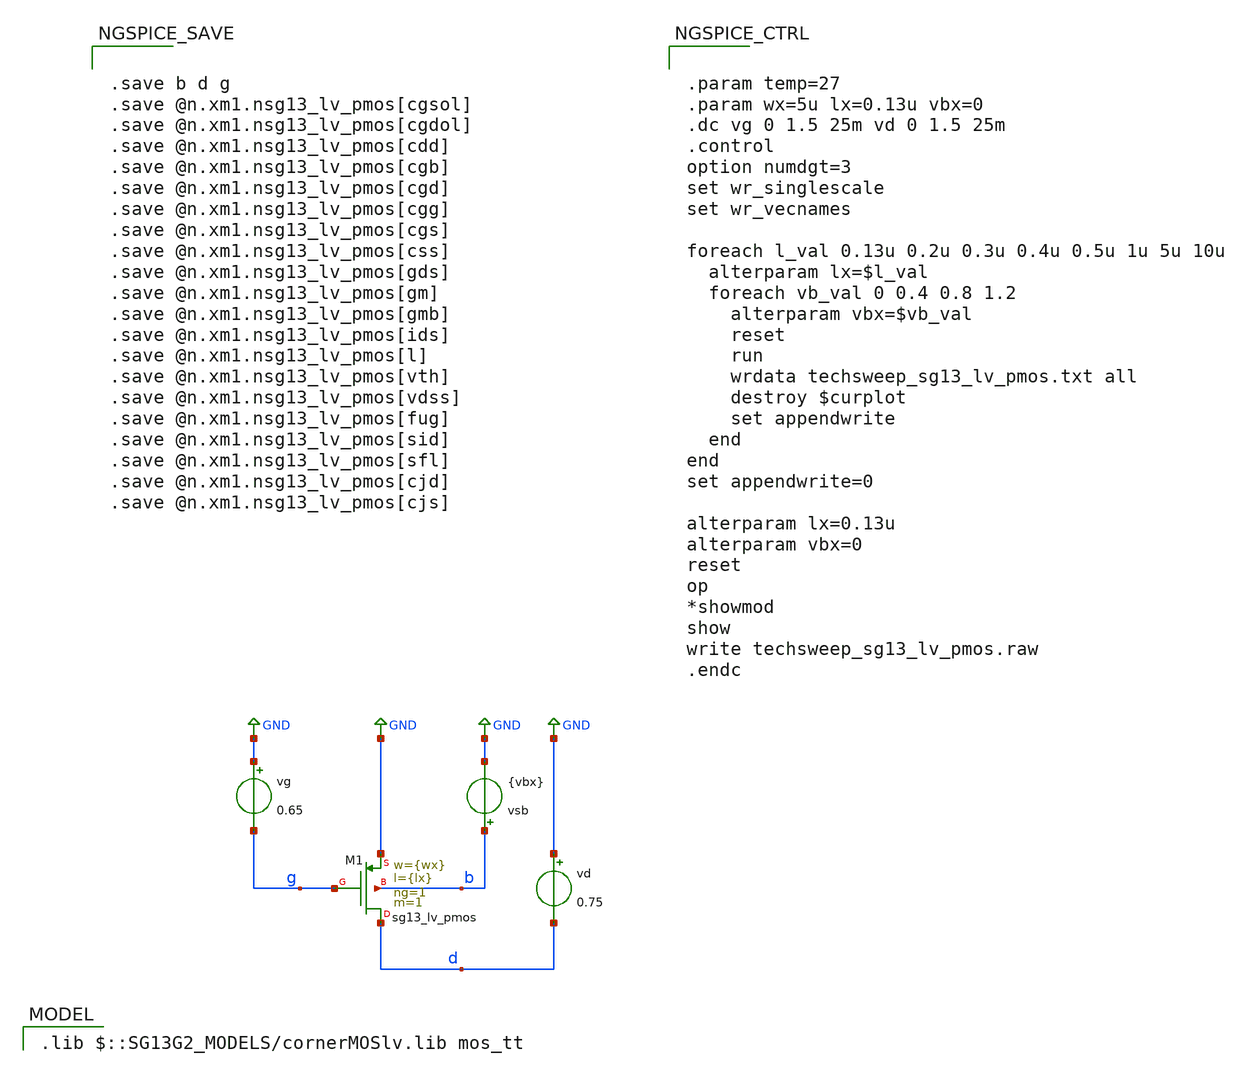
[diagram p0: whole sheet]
** sch_path: xschem/techsweep_sg13g2_lv_pmos.sch
* (c) 2024 Harald Pretl (adapted from Boris Murmann)
**.subckt techsweep_sg13g2_lv_pmos
XM1 d g GND b sg13_lv_pmos w={wx} l={lx} ng=1 m=1 mm_ok=1
vd GND d 0.75
vsb b GND {vbx}
vg GND g 0.65
**** begin user architecture code
 .lib $::SG13G2_MODELS/cornerMOSlv.lib mos_tt



.param temp=27
.param wx=5u lx=0.13u vbx=0
.dc vg 0 1.5 25m vd 0 1.5 25m
.control
option numdgt=3
set wr_singlescale
set wr_vecnames

foreach l_val 0.13u 0.2u 0.3u 0.4u 0.5u 1u 5u 10u
  alterparam lx=$l_val
  foreach vb_val 0 0.4 0.8 1.2
    alterparam vbx=$vb_val
    reset
    run
    wrdata techsweep_sg13_lv_pmos.txt all
    destroy $curplot
    set appendwrite
  end
end
set appendwrite=0

alterparam lx=0.13u
alterparam vbx=0
reset
op
*showmod
show
write techsweep_sg13_lv_pmos.raw
.endc




.save b d g
.save @n.xm1.nsg13_lv_pmos[cgsol]
.save @n.xm1.nsg13_lv_pmos[cgdol]
.save @n.xm1.nsg13_lv_pmos[cdd]
.save @n.xm1.nsg13_lv_pmos[cgb]
.save @n.xm1.nsg13_lv_pmos[cgd]
.save @n.xm1.nsg13_lv_pmos[cgg]
.save @n.xm1.nsg13_lv_pmos[cgs]
.save @n.xm1.nsg13_lv_pmos[css]
.save @n.xm1.nsg13_lv_pmos[gds]
.save @n.xm1.nsg13_lv_pmos[gm]
.save @n.xm1.nsg13_lv_pmos[gmb]
.save @n.xm1.nsg13_lv_pmos[ids]
.save @n.xm1.nsg13_lv_pmos[l]
.save @n.xm1.nsg13_lv_pmos[vth]
.save @n.xm1.nsg13_lv_pmos[vdss]
.save @n.xm1.nsg13_lv_pmos[fug]
.save @n.xm1.nsg13_lv_pmos[sid]
.save @n.xm1.nsg13_lv_pmos[sfl]
.save @n.xm1.nsg13_lv_pmos[cjd]
.save @n.xm1.nsg13_lv_pmos[cjs]


**** end user architecture code
**.ends
.GLOBAL GND
.end
